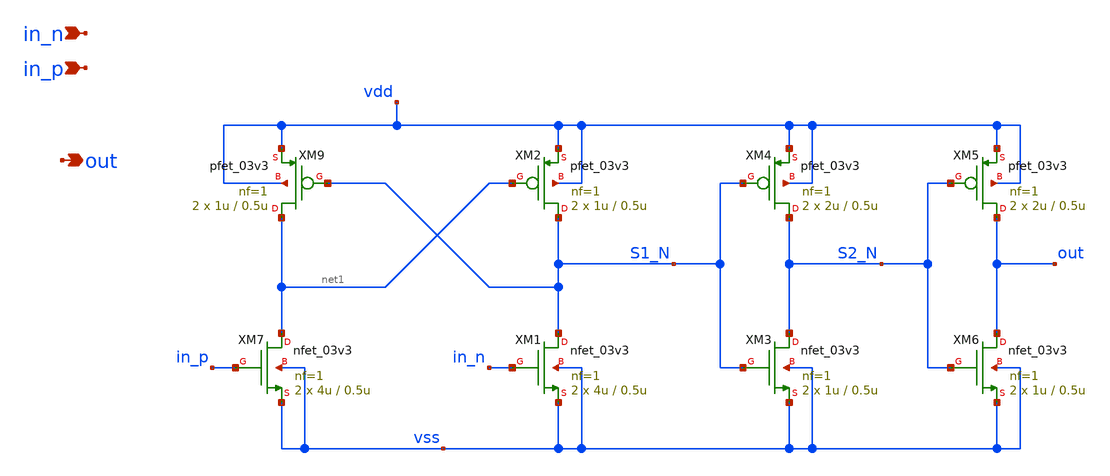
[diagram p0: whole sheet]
** sch_path: xschem/level_shift.sch
**.subckt level_shift in_n in_p out
*.ipin in_n
*.ipin in_p
*.opin out
XM9 net1 S1_N vdd vdd pfet_03v3 L=0.5u W=1u nf=1 ad='int((nf+1)/2) * W/nf * 0.18u' as='int((nf+2)/2) * W/nf * 0.18u'
+ pd='2*int((nf+1)/2) * (W/nf + 0.18u)' ps='2*int((nf+2)/2) * (W/nf + 0.18u)' nrd='0.18u / W' nrs='0.18u / W'
+ sa=0 sb=0 sd=0 m=2 par=2
XM2 S1_N net1 vdd vdd pfet_03v3 L=0.5u W=1u nf=1 ad='int((nf+1)/2) * W/nf * 0.18u' as='int((nf+2)/2) * W/nf * 0.18u'
+ pd='2*int((nf+1)/2) * (W/nf + 0.18u)' ps='2*int((nf+2)/2) * (W/nf + 0.18u)' nrd='0.18u / W' nrs='0.18u / W'
+ sa=0 sb=0 sd=0 m=2 par=2
XM4 S2_N S1_N vdd vdd pfet_03v3 L=0.5u W=2u nf=1 ad='int((nf+1)/2) * W/nf * 0.18u' as='int((nf+2)/2) * W/nf * 0.18u'
+ pd='2*int((nf+1)/2) * (W/nf + 0.18u)' ps='2*int((nf+2)/2) * (W/nf + 0.18u)' nrd='0.18u / W' nrs='0.18u / W'
+ sa=0 sb=0 sd=0 m=2 par=2
XM5 out S2_N vdd vdd pfet_03v3 L=0.5u W=2u nf=1 ad='int((nf+1)/2) * W/nf * 0.18u' as='int((nf+2)/2) * W/nf * 0.18u'
+ pd='2*int((nf+1)/2) * (W/nf + 0.18u)' ps='2*int((nf+2)/2) * (W/nf + 0.18u)' nrd='0.18u / W' nrs='0.18u / W'
+ sa=0 sb=0 sd=0 m=2 par=2
XM7 net1 in_p vss vss nfet_03v3 L=0.5u W=4u nf=1 ad='int((nf+1)/2) * W/nf * 0.18u' as='int((nf+2)/2) * W/nf * 0.18u'
+ pd='2*int((nf+1)/2) * (W/nf + 0.18u)' ps='2*int((nf+2)/2) * (W/nf + 0.18u)' nrd='0.18u / W' nrs='0.18u / W'
+ sa=0 sb=0 sd=0 m=2 par=2
XM1 S1_N in_n vss vss nfet_03v3 L=0.5u W=4u nf=1 ad='int((nf+1)/2) * W/nf * 0.18u' as='int((nf+2)/2) * W/nf * 0.18u'
+ pd='2*int((nf+1)/2) * (W/nf + 0.18u)' ps='2*int((nf+2)/2) * (W/nf + 0.18u)' nrd='0.18u / W' nrs='0.18u / W'
+ sa=0 sb=0 sd=0 m=2 par=2
XM3 S2_N S1_N vss vss nfet_03v3 L=0.5u W=1u nf=1 ad='int((nf+1)/2) * W/nf * 0.18u' as='int((nf+2)/2) * W/nf * 0.18u'
+ pd='2*int((nf+1)/2) * (W/nf + 0.18u)' ps='2*int((nf+2)/2) * (W/nf + 0.18u)' nrd='0.18u / W' nrs='0.18u / W'
+ sa=0 sb=0 sd=0 m=2 par=2
XM6 out S2_N vss vss nfet_03v3 L=0.5u W=1u nf=1 ad='int((nf+1)/2) * W/nf * 0.18u' as='int((nf+2)/2) * W/nf * 0.18u'
+ pd='2*int((nf+1)/2) * (W/nf + 0.18u)' ps='2*int((nf+2)/2) * (W/nf + 0.18u)' nrd='0.18u / W' nrs='0.18u / W'
+ sa=0 sb=0 sd=0 m=2 par=2
**.ends
.end
